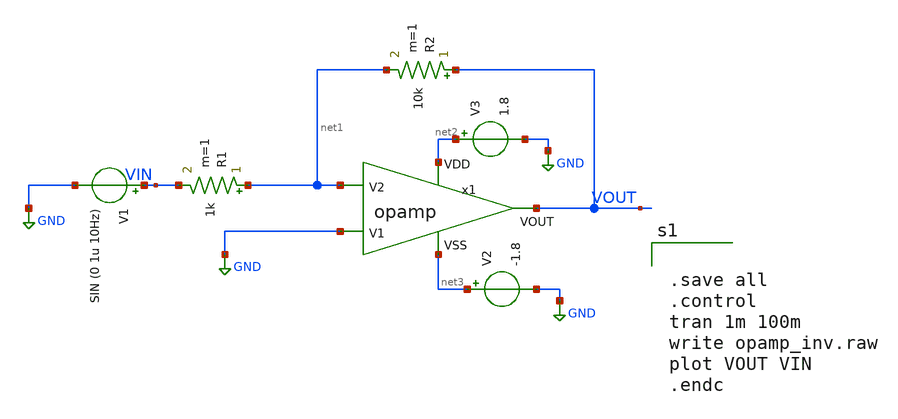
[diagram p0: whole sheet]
** sch_path: xschem/opamp_inv_fs.sch
**.subckt opamp_inv_fs
V1 VIN GND SIN (0 1u 10Hz)
V2 net3 GND -1.8
V3 net2 GND 1.8
R1 net1 VIN 1k m=1
R2 VOUT net1 10k m=1
x1 net2 net3 GND net1 VOUT opamp
**** begin user architecture code


.save all
.control
tran 1m 100m
write opamp_inv.raw
plot VOUT VIN
.endc



** opencircuitdesign pdks install
.lib $::SKYWATER_MODELS/sky130.lib.spice fs


**** end user architecture code
**.ends

* expanding   symbol:  /foss/designs/chipalooza2024/sky130_hcmus_ip__instramp/xschem/opamp.sym # of
*+ pins=5
** sym_path: /foss/designs/chipalooza2024/sky130_hcmus_ip__instramp/xschem/opamp.sym
** sch_path: /foss/designs/chipalooza2024/sky130_hcmus_ip__instramp/xschem/opamp.sch
.subckt opamp VDD VSS V1 V2 VOUT
*.ipin VSS
*.ipin VDD
*.ipin V2
*.ipin V1
*.opin VOUT
XM2 net5 V2 net1 VSS sky130_fd_pr__nfet_g5v0d10v5 L=1 W=18 nf=1 ad='int((nf+1)/2) * W/nf * 0.29' as='int((nf+2)/2) * W/nf * 0.29'
+ pd='2*int((nf+1)/2) * (W/nf + 0.29)' ps='2*int((nf+2)/2) * (W/nf + 0.29)' nrd='0.29 / W' nrs='0.29 / W'
+ sa=0 sb=0 sd=0 mult=1 m=1
XM1 net6 net5 VDD VDD sky130_fd_pr__pfet_g5v0d10v5 L=1 W=30 nf=1 ad='int((nf+1)/2) * W/nf * 0.29' as='int((nf+2)/2) * W/nf * 0.29'
+ pd='2*int((nf+1)/2) * (W/nf + 0.29)' ps='2*int((nf+2)/2) * (W/nf + 0.29)' nrd='0.29 / W' nrs='0.29 / W'
+ sa=0 sb=0 sd=0 mult=1 m=1
XM4 net6 V1 net1 VSS sky130_fd_pr__nfet_g5v0d10v5 L=1 W=18 nf=1 ad='int((nf+1)/2) * W/nf * 0.29' as='int((nf+2)/2) * W/nf * 0.29'
+ pd='2*int((nf+1)/2) * (W/nf + 0.29)' ps='2*int((nf+2)/2) * (W/nf + 0.29)' nrd='0.29 / W' nrs='0.29 / W'
+ sa=0 sb=0 sd=0 mult=1 m=1
XM5 net1 net4 VSS VSS sky130_fd_pr__nfet_g5v0d10v5 L=1 W=15.171 nf=1 ad='int((nf+1)/2) * W/nf * 0.29'
+ as='int((nf+2)/2) * W/nf * 0.29' pd='2*int((nf+1)/2) * (W/nf + 0.29)' ps='2*int((nf+2)/2) * (W/nf + 0.29)'
+ nrd='0.29 / W' nrs='0.29 / W' sa=0 sb=0 sd=0 mult=1 m=1
XM6 VOUT net4 VSS VSS sky130_fd_pr__nfet_g5v0d10v5 L=1 W=19 nf=1 ad='int((nf+1)/2) * W/nf * 0.29' as='int((nf+2)/2) * W/nf * 0.29'
+ pd='2*int((nf+1)/2) * (W/nf + 0.29)' ps='2*int((nf+2)/2) * (W/nf + 0.29)' nrd='0.29 / W' nrs='0.29 / W'
+ sa=0 sb=0 sd=0 mult=1 m=1
XM7 net4 net4 VSS VSS sky130_fd_pr__nfet_g5v0d10v5 L=1 W=20 nf=1 ad='int((nf+1)/2) * W/nf * 0.29' as='int((nf+2)/2) * W/nf * 0.29'
+ pd='2*int((nf+1)/2) * (W/nf + 0.29)' ps='2*int((nf+2)/2) * (W/nf + 0.29)' nrd='0.29 / W' nrs='0.29 / W'
+ sa=0 sb=0 sd=0 mult=1 m=1
XM3 net5 net5 VDD VDD sky130_fd_pr__pfet_g5v0d10v5 L=1 W=30 nf=1 ad='int((nf+1)/2) * W/nf * 0.29' as='int((nf+2)/2) * W/nf * 0.29'
+ pd='2*int((nf+1)/2) * (W/nf + 0.29)' ps='2*int((nf+2)/2) * (W/nf + 0.29)' nrd='0.29 / W' nrs='0.29 / W'
+ sa=0 sb=0 sd=0 mult=1 m=1
XM8 VOUT net6 VDD VDD sky130_fd_pr__pfet_g5v0d10v5 L=1 W=38 nf=1 ad='int((nf+1)/2) * W/nf * 0.29' as='int((nf+2)/2) * W/nf * 0.29'
+ pd='2*int((nf+1)/2) * (W/nf + 0.29)' ps='2*int((nf+2)/2) * (W/nf + 0.29)' nrd='0.29 / W' nrs='0.29 / W'
+ sa=0 sb=0 sd=0 mult=2 m=2
XR3 net2 VDD VSS sky130_fd_pr__res_high_po W=1 L=30 mult=1 m=1
XR1 net3 net2 VSS sky130_fd_pr__res_high_po W=1 L=30 mult=1 m=1
XR2 net4 net3 VSS sky130_fd_pr__res_high_po W=1 L=30 mult=1 m=1
XR4 net7 VOUT VSS sky130_fd_pr__res_high_po W=1 L=5 mult=1 m=1
XC1 net7 net6 sky130_fd_pr__cap_mim_m3_1 W=5.5 L=10 MF=10 m=10
.ends

.GLOBAL GND
.end
